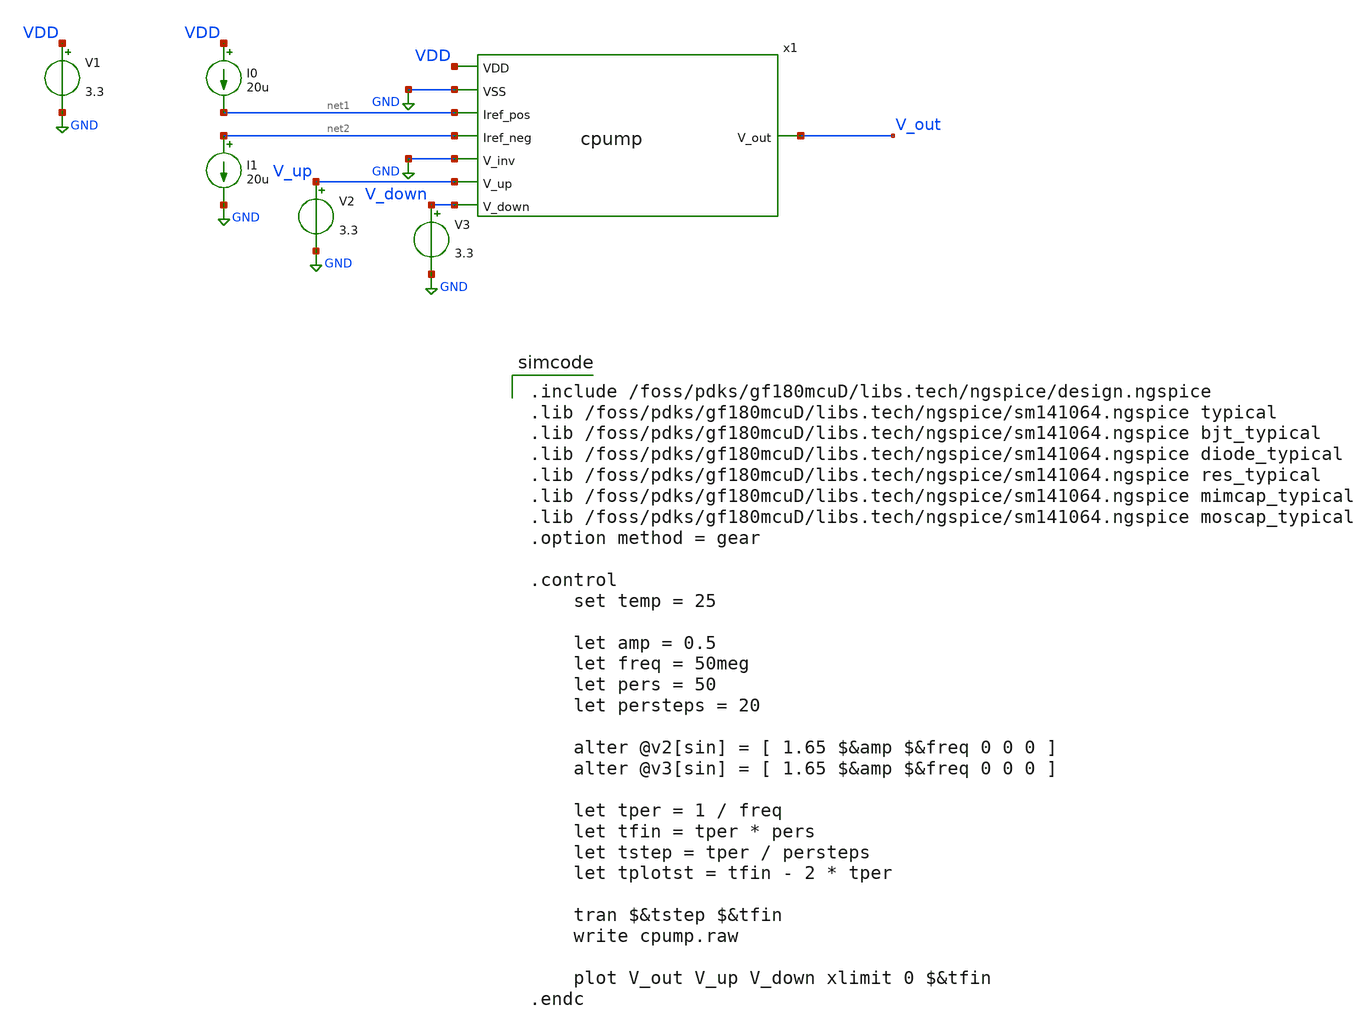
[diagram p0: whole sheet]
** sch_path: blocks/pll/cpump_tb.sch
**.subckt cpump_tb
x1 net1 VDD V_up V_out V_down GND net2 cpump
V1 VDD GND 3.3
I0 VDD net1 20u
I1 net2 GND 20u
V2 V_up GND 3.3
V3 V_down GND 3.3
**** begin user architecture code

.include /foss/pdks/gf180mcuD/libs.tech/ngspice/design.ngspice
.lib /foss/pdks/gf180mcuD/libs.tech/ngspice/sm141064.ngspice typical
.lib /foss/pdks/gf180mcuD/libs.tech/ngspice/sm141064.ngspice bjt_typical
.lib /foss/pdks/gf180mcuD/libs.tech/ngspice/sm141064.ngspice diode_typical
.lib /foss/pdks/gf180mcuD/libs.tech/ngspice/sm141064.ngspice res_typical
.lib /foss/pdks/gf180mcuD/libs.tech/ngspice/sm141064.ngspice mimcap_typical
.lib /foss/pdks/gf180mcuD/libs.tech/ngspice/sm141064.ngspice moscap_typical
.option method = gear

.control
    set temp = 25

    let amp = 0.5
    let freq = 50meg
    let pers = 50
    let persteps = 20

    alter @v2[sin] = [ 1.65 $&amp $&freq 0 0 0 ]
    alter @v3[sin] = [ 1.65 $&amp $&freq 0 0 0 ]

    let tper = 1 / freq
    let tfin = tper * pers
    let tstep = tper / persteps
    let tplotst = tfin - 2 * tper

    tran $&tstep $&tfin
    write cpump.raw

    plot V_out V_up V_down xlimit 0 $&tfin
.endc


**** end user architecture code
**.ends

* expanding   symbol:  blocks/pll/cpump.sym # of pins=8
** sym_path: blocks/pll/cpump.sym
** sch_path: blocks/pll/cpump.sch
.subckt cpump Iref_pos VDD V_up V_out V_down VSS Iref_neg
*.ipin Iref_pos
*.ipin Iref_neg
*.ipin V_up
*.ipin V_down
*.ipin V_inv
*.ipin VDD
*.ipin VSS
*.opin V_out
XM1 V_out V_up Iref_pos VDD pfet_03v3 L=1u W=40u nf=10 ad='int((nf+1)/2) * W/nf * 0.18u' as='int((nf+2)/2) * W/nf * 0.18u'
+ pd='2*int((nf+1)/2) * (W/nf + 0.18u)' ps='2*int((nf+2)/2) * (W/nf + 0.18u)' nrd='0.18u / W' nrs='0.18u / W'
+ sa=0 sb=0 sd=0 m=1
XM2 V_out V_down Iref_neg VSS nfet_03v3 L=1u W=4u nf=1 ad='int((nf+1)/2) * W/nf * 0.18u' as='int((nf+2)/2) * W/nf * 0.18u'
+ pd='2*int((nf+1)/2) * (W/nf + 0.18u)' ps='2*int((nf+2)/2) * (W/nf + 0.18u)' nrd='0.18u / W' nrs='0.18u / W'
+ sa=0 sb=0 sd=0 m=1
XR1 net1 V_out VSS ppolyf_u r_width=2e-6 r_length=8e-6 m=1
XC3 V_inv VSS cap_nmos_03v3 c_width=1e-6 c_length=1e-6 m=1
XC1 net1 VSS cap_mim_2f0_m4m5_noshield c_width=5e-6 c_length=5e-6 m=1
XC2 V_out VSS cap_mim_2f0_m4m5_noshield c_width=5e-6 c_length=5e-6 m=1
.ends

.GLOBAL GND
.end
